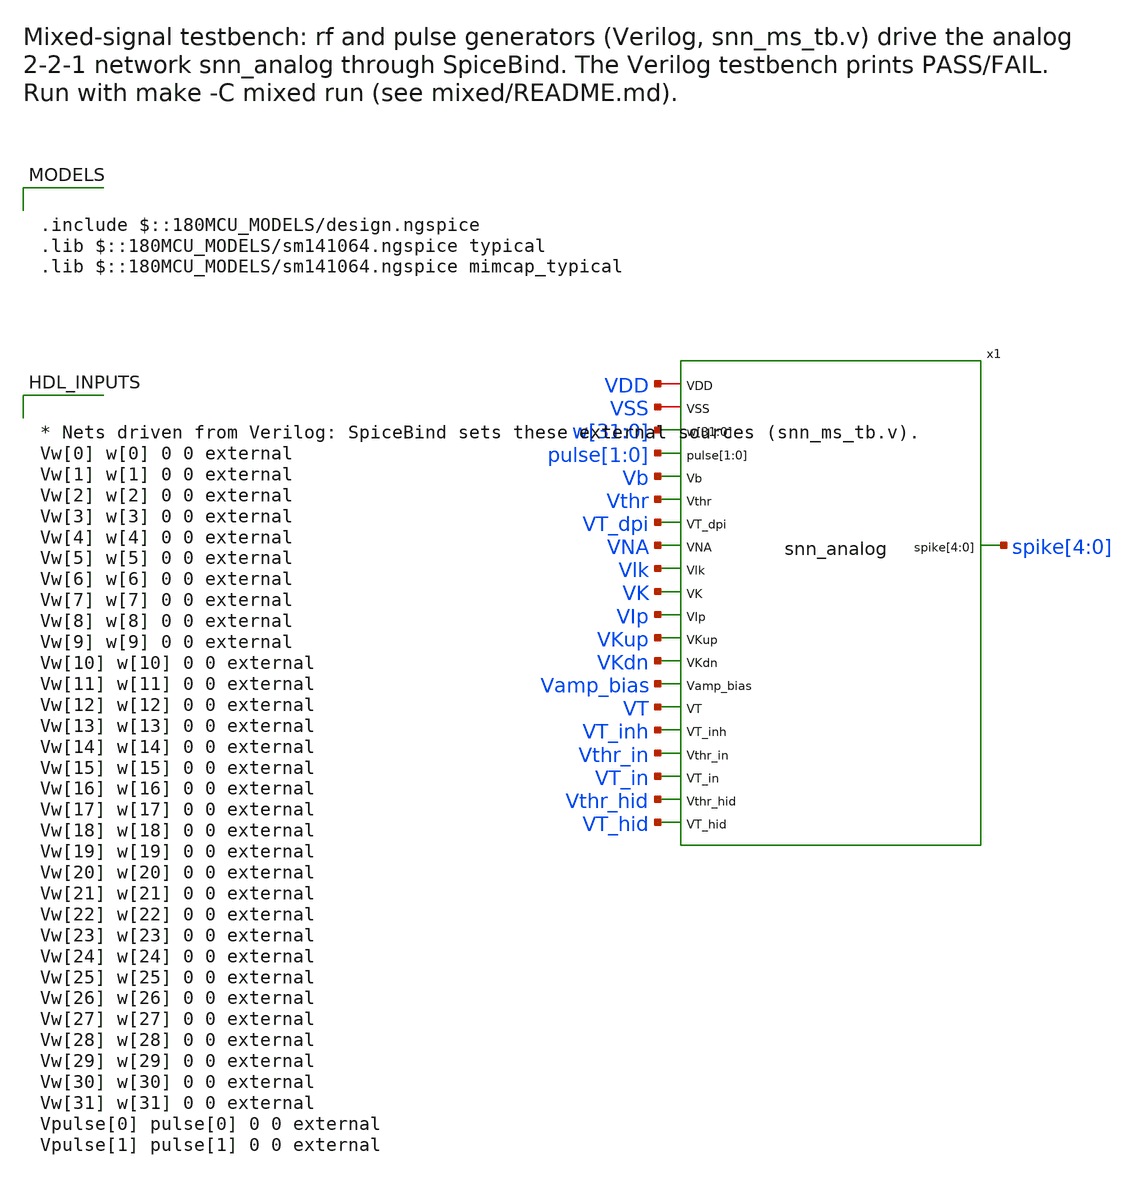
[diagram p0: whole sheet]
** sch_path: mixed/snn_ms_tb.sch
**.subckt snn_ms_tb
x1 VDD VSS w[31] w[30] w[29] w[28] w[27] w[26] w[25] w[24] w[23] w[22] w[21] w[20] w[19] w[18] w[17]
+ w[16] w[15] w[14] w[13] w[12] w[11] w[10] w[9] w[8] w[7] w[6] w[5] w[4] w[3] w[2] w[1] w[0] pulse[1]
+ pulse[0] Vb Vthr VT_dpi VNA Vlk VK VIp VKup VKdn Vamp_bias VT VT_inh Vthr_in VT_in Vthr_hid VT_hid spike[4]
+ spike[3] spike[2] spike[1] spike[0] snn_analog
**** begin user architecture code

.include $::180MCU_MODELS/design.ngspice
.lib $::180MCU_MODELS/sm141064.ngspice typical
.lib $::180MCU_MODELS/sm141064.ngspice mimcap_typical



* Nets driven from Verilog: SpiceBind sets these external sources (snn_ms_tb.v).
Vw[0] w[0] 0 0 external
Vw[1] w[1] 0 0 external
Vw[2] w[2] 0 0 external
Vw[3] w[3] 0 0 external
Vw[4] w[4] 0 0 external
Vw[5] w[5] 0 0 external
Vw[6] w[6] 0 0 external
Vw[7] w[7] 0 0 external
Vw[8] w[8] 0 0 external
Vw[9] w[9] 0 0 external
Vw[10] w[10] 0 0 external
Vw[11] w[11] 0 0 external
Vw[12] w[12] 0 0 external
Vw[13] w[13] 0 0 external
Vw[14] w[14] 0 0 external
Vw[15] w[15] 0 0 external
Vw[16] w[16] 0 0 external
Vw[17] w[17] 0 0 external
Vw[18] w[18] 0 0 external
Vw[19] w[19] 0 0 external
Vw[20] w[20] 0 0 external
Vw[21] w[21] 0 0 external
Vw[22] w[22] 0 0 external
Vw[23] w[23] 0 0 external
Vw[24] w[24] 0 0 external
Vw[25] w[25] 0 0 external
Vw[26] w[26] 0 0 external
Vw[27] w[27] 0 0 external
Vw[28] w[28] 0 0 external
Vw[29] w[29] 0 0 external
Vw[30] w[30] 0 0 external
Vw[31] w[31] 0 0 external
Vpulse[0] pulse[0] 0 0 external
Vpulse[1] pulse[1] 0 0 external




* Supplies and biases: the XOR operating point of analog/testbenches/xor/xor_tb.sch
* (fixed voltages, tt; see analog/testbenches/xor/README.md). Per-layer DPI biases:
* inputs Vthr_in / VT_in, hidden Vthr_hid / VT_hid, output Vthr / VT_dpi (VT_inh: output
*+ inhibition).
* Parameter names start with p_: a .param with the same name as a net made ngspice
* rename that net to {name} on the long x1 line, leaving the biases unconnected.
.param p_vdd=3.3 p_iref=14.42n
.param p_vthr=2.70 p_vtau=0.5096 p_vtau_i=0.5096
.param p_vthr_in=2.4 p_vtau_in=0.695 p_vthr_hid=2.5 p_vtau_hid=0.655
.param p_vlk=0.48 p_vamp_bias=0.535 p_vip=0.573 p_vna=1.93 p_vkup=2.35 p_vk=1.22 p_vkdn=0.588
+ p_vt=1.66
Vdd VDD 0 {p_vdd}
Vss VSS 0 0
* DAC unit current: Iref into a diode-connected unit current source (w[0] = 15 nA)
Iref VDD Vb {p_iref}
XMref Vb Vb 0 0 nfet_03v3 L=8u W=1u nf=1
* VT_* are source-gate voltages of the DPI tau pFET (VT = VDD - p_vtau)
Vthr Vthr 0 {p_vthr}
Vtau VDD VT_dpi {p_vtau}
Vtau_i VDD VT_inh {p_vtau_i}
Vthr_in Vthr_in 0 {p_vthr_in}
Vtau_in VDD VT_in {p_vtau_in}
Vthr_hid Vthr_hid 0 {p_vthr_hid}
Vtau_hid VDD VT_hid {p_vtau_hid}
Vlk Vlk VSS {p_vlk}
VK VK VSS {p_vk}
VNA VNA VSS {p_vna}
VKup VKup VSS {p_vkup}
VKdn VKdn VSS {p_vkdn}
VIp VIp VSS {p_vip}
VT VT VSS {p_vt}
Vamp_bias Vamp_bias VSS {p_vamp_bias}
* Without this the DC operating point of the sized network does not converge
.ic v(x1.VMEM_0)=0 v(x1.VMEM_1)=0 v(x1.VMEM_2)=0 v(x1.VMEM_3)=0 v(x1.VMEM_4)=0 v(spike[0])=0
+ v(spike[1])=0 v(spike[2])=0 v(spike[3])=0 v(spike[4])=0




* Gear integration: trap makes the DPI output current ring after each reset (entry 46)
.options method=gear
.save v(spike[0]) v(spike[1]) v(spike[2]) v(spike[3]) v(spike[4]) v(pulse[0]) v(pulse[1]) v(x1.VMEM_0) v(x1.VMEM_1) v(x1.VMEM_2) v(x1.VMEM_3) v(x1.VMEM_4)
* Runs until the Verilog testbench calls $finish. ngspice reserves memory for tstop/step
* points, so a huge bound crashes it (1 s did): keep this just above the longest run.
.tran 0.1u 100m 0 0.1u


**** end user architecture code
**.ends
.end
